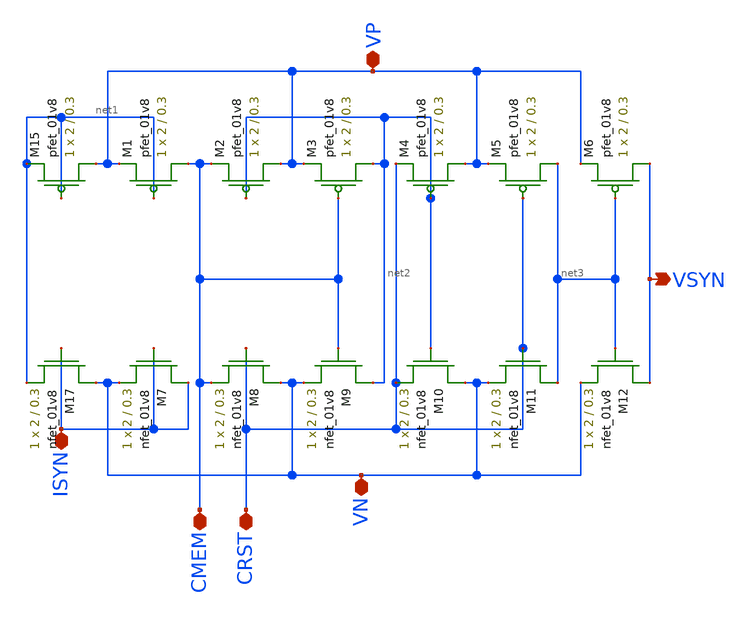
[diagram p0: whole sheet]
** sch_path: schematic/besrour_neuron_cm_lds_lvs.sch
**.subckt besrour_neuron_cm_lds_lvs VP VN ISYN VSYN CRST CMEM
*.iopin VP
*.iopin VN
*.iopin ISYN
*.opin VSYN
*.iopin CRST
*.iopin CMEM
XM15 VP net1 net1 VP sky130_fd_pr__pfet_01v8 L=0.3 W=2 nf=1 ad='int((nf+1)/2) * W/nf * 0.29' as='int((nf+2)/2) * W/nf * 0.29'
+ pd='2*int((nf+1)/2) * (W/nf + 0.29)' ps='2*int((nf+2)/2) * (W/nf + 0.29)' nrd='0.29 / W' nrs='0.29 / W'
+ sa=0 sb=0 sd=0 mult=1 m=1
XM17 VN ISYN net1 VN sky130_fd_pr__nfet_01v8 L=0.3 W=2 nf=1 ad='int((nf+1)/2) * W/nf * 0.29' as='int((nf+2)/2) * W/nf * 0.29'
+ pd='2*int((nf+1)/2) * (W/nf + 0.29)' ps='2*int((nf+2)/2) * (W/nf + 0.29)' nrd='0.29 / W' nrs='0.29 / W'
+ sa=0 sb=0 sd=0 mult=1 m=1
XM7 ISYN ISYN VN VN sky130_fd_pr__nfet_01v8 L=0.3 W=2 nf=1 ad='int((nf+1)/2) * W/nf * 0.29' as='int((nf+2)/2) * W/nf * 0.29'
+ pd='2*int((nf+1)/2) * (W/nf + 0.29)' ps='2*int((nf+2)/2) * (W/nf + 0.29)' nrd='0.29 / W' nrs='0.29 / W'
+ sa=0 sb=0 sd=0 mult=1 m=1
XM8 VN CRST CMEM VN sky130_fd_pr__nfet_01v8 L=0.3 W=2 nf=1 ad='int((nf+1)/2) * W/nf * 0.29' as='int((nf+2)/2) * W/nf * 0.29'
+ pd='2*int((nf+1)/2) * (W/nf + 0.29)' ps='2*int((nf+2)/2) * (W/nf + 0.29)' nrd='0.29 / W' nrs='0.29 / W'
+ sa=0 sb=0 sd=0 mult=1 m=1
XM9 net2 CMEM VN VN sky130_fd_pr__nfet_01v8 L=0.3 W=2 nf=1 ad='int((nf+1)/2) * W/nf * 0.29' as='int((nf+2)/2) * W/nf * 0.29'
+ pd='2*int((nf+1)/2) * (W/nf + 0.29)' ps='2*int((nf+2)/2) * (W/nf + 0.29)' nrd='0.29 / W' nrs='0.29 / W'
+ sa=0 sb=0 sd=0 mult=1 m=1
XM10 VN net2 CRST VN sky130_fd_pr__nfet_01v8 L=0.3 W=2 nf=1 ad='int((nf+1)/2) * W/nf * 0.29' as='int((nf+2)/2) * W/nf * 0.29'
+ pd='2*int((nf+1)/2) * (W/nf + 0.29)' ps='2*int((nf+2)/2) * (W/nf + 0.29)' nrd='0.29 / W' nrs='0.29 / W'
+ sa=0 sb=0 sd=0 mult=1 m=1
XM11 net3 CRST VN VN sky130_fd_pr__nfet_01v8 L=0.3 W=2 nf=1 ad='int((nf+1)/2) * W/nf * 0.29' as='int((nf+2)/2) * W/nf * 0.29'
+ pd='2*int((nf+1)/2) * (W/nf + 0.29)' ps='2*int((nf+2)/2) * (W/nf + 0.29)' nrd='0.29 / W' nrs='0.29 / W'
+ sa=0 sb=0 sd=0 mult=1 m=1
XM12 VSYN net3 VN VN sky130_fd_pr__nfet_01v8 L=0.3 W=2 nf=1 ad='int((nf+1)/2) * W/nf * 0.29' as='int((nf+2)/2) * W/nf * 0.29'
+ pd='2*int((nf+1)/2) * (W/nf + 0.29)' ps='2*int((nf+2)/2) * (W/nf + 0.29)' nrd='0.29 / W' nrs='0.29 / W'
+ sa=0 sb=0 sd=0 mult=1 m=1
XM1 CMEM net1 VP VP sky130_fd_pr__pfet_01v8 L=0.3 W=2 nf=1 ad='int((nf+1)/2) * W/nf * 0.29' as='int((nf+2)/2) * W/nf * 0.29'
+ pd='2*int((nf+1)/2) * (W/nf + 0.29)' ps='2*int((nf+2)/2) * (W/nf + 0.29)' nrd='0.29 / W' nrs='0.29 / W'
+ sa=0 sb=0 sd=0 mult=1 m=1
XM2 VP net2 CMEM VP sky130_fd_pr__pfet_01v8 L=0.3 W=2 nf=1 ad='int((nf+1)/2) * W/nf * 0.29' as='int((nf+2)/2) * W/nf * 0.29'
+ pd='2*int((nf+1)/2) * (W/nf + 0.29)' ps='2*int((nf+2)/2) * (W/nf + 0.29)' nrd='0.29 / W' nrs='0.29 / W'
+ sa=0 sb=0 sd=0 mult=1 m=1
XM3 net2 CMEM VP VP sky130_fd_pr__pfet_01v8 L=0.3 W=2 nf=1 ad='int((nf+1)/2) * W/nf * 0.29' as='int((nf+2)/2) * W/nf * 0.29'
+ pd='2*int((nf+1)/2) * (W/nf + 0.29)' ps='2*int((nf+2)/2) * (W/nf + 0.29)' nrd='0.29 / W' nrs='0.29 / W'
+ sa=0 sb=0 sd=0 mult=1 m=1
XM4 VP net2 CRST VP sky130_fd_pr__pfet_01v8 L=0.3 W=2 nf=1 ad='int((nf+1)/2) * W/nf * 0.29' as='int((nf+2)/2) * W/nf * 0.29'
+ pd='2*int((nf+1)/2) * (W/nf + 0.29)' ps='2*int((nf+2)/2) * (W/nf + 0.29)' nrd='0.29 / W' nrs='0.29 / W'
+ sa=0 sb=0 sd=0 mult=1 m=1
XM5 net3 CRST VP VP sky130_fd_pr__pfet_01v8 L=0.3 W=2 nf=1 ad='int((nf+1)/2) * W/nf * 0.29' as='int((nf+2)/2) * W/nf * 0.29'
+ pd='2*int((nf+1)/2) * (W/nf + 0.29)' ps='2*int((nf+2)/2) * (W/nf + 0.29)' nrd='0.29 / W' nrs='0.29 / W'
+ sa=0 sb=0 sd=0 mult=1 m=1
XM6 VSYN net3 VP VP sky130_fd_pr__pfet_01v8 L=0.3 W=2 nf=1 ad='int((nf+1)/2) * W/nf * 0.29' as='int((nf+2)/2) * W/nf * 0.29'
+ pd='2*int((nf+1)/2) * (W/nf + 0.29)' ps='2*int((nf+2)/2) * (W/nf + 0.29)' nrd='0.29 / W' nrs='0.29 / W'
+ sa=0 sb=0 sd=0 mult=1 m=1
**.ends
.end
